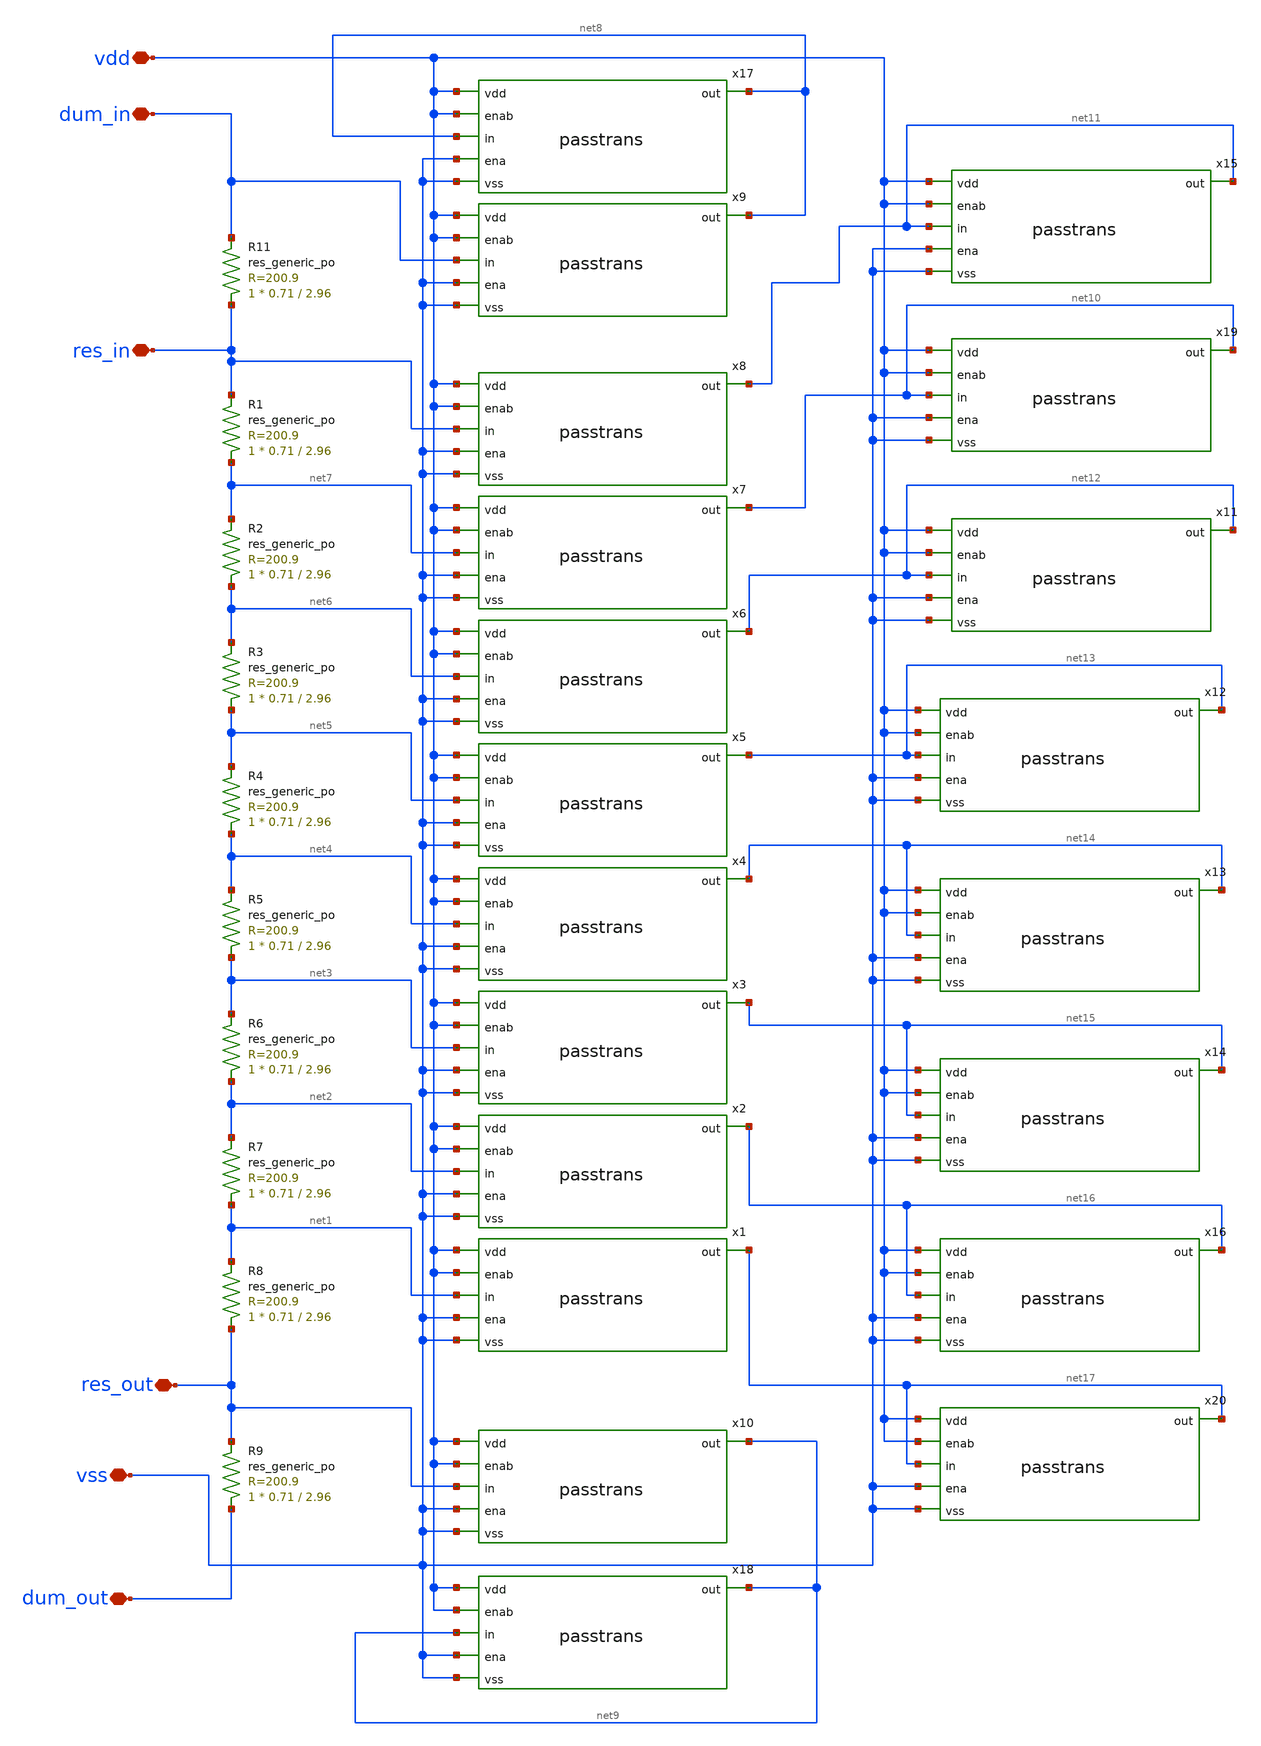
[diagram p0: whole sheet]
** sch_path: xschem/rheo_column_dummy.sch
**.subckt rheo_column_dummy res_in vss vdd dum_in res_out dum_out
*.iopin res_in
*.iopin vss
*.iopin vdd
*.iopin dum_in
*.iopin res_out
*.iopin dum_out
x1 vdd vdd net17 net1 vss vss passtrans
x2 vdd vdd net16 net2 vss vss passtrans
x3 vdd vdd net15 net3 vss vss passtrans
x4 vdd vdd net14 net4 vss vss passtrans
x5 vdd vdd net13 net5 vss vss passtrans
x6 vdd vdd net12 net6 vss vss passtrans
x7 vdd vdd net10 net7 vss vss passtrans
x8 vdd vdd net11 res_in vss vss passtrans
x9 vdd vdd net8 dum_in vss vss passtrans
x10 vdd vdd net9 res_out vss vss passtrans
x11 vdd vdd net12 net12 vss vss passtrans
x12 vdd vdd net13 net13 vss vss passtrans
x13 vdd vdd net14 net14 vss vss passtrans
x14 vdd vdd net15 net15 vss vss passtrans
x15 vdd vdd net11 net11 vss vss passtrans
x16 vdd vdd net16 net16 vss vss passtrans
x17 vdd vdd net8 net8 vss vss passtrans
x18 vdd vdd net9 net9 vss vss passtrans
x19 vdd vdd net10 net10 vss vss passtrans
x20 vdd vdd net17 net17 vss vss passtrans
XR11 res_in dum_in sky130_fd_pr__res_generic_po W=0.71 L=2.96 m=1
XR1 net7 res_in sky130_fd_pr__res_generic_po W=0.71 L=2.96 m=1
XR2 net6 net7 sky130_fd_pr__res_generic_po W=0.71 L=2.96 m=1
XR3 net5 net6 sky130_fd_pr__res_generic_po W=0.71 L=2.96 m=1
XR4 net4 net5 sky130_fd_pr__res_generic_po W=0.71 L=2.96 m=1
XR5 net3 net4 sky130_fd_pr__res_generic_po W=0.71 L=2.96 m=1
XR6 net2 net3 sky130_fd_pr__res_generic_po W=0.71 L=2.96 m=1
XR7 net1 net2 sky130_fd_pr__res_generic_po W=0.71 L=2.96 m=1
XR8 res_out net1 sky130_fd_pr__res_generic_po W=0.71 L=2.96 m=1
XR9 dum_out res_out sky130_fd_pr__res_generic_po W=0.71 L=2.96 m=1
**.ends

* expanding   symbol:  passtrans.sym # of pins=6
** sym_path: xschem/passtrans.sym
** sch_path: xschem/passtrans.sch
.subckt passtrans vdd enab out in ena vss
*.ipin enab
*.ipin ena
*.ipin vss
*.ipin vdd
*.iopin in
*.iopin out
XM1 in ena out vss sky130_fd_pr__nfet_g5v0d10v5 L=0.5 W=0.65 nf=1 ad='int((nf+1)/2) * W/nf * 0.29' as='int((nf+2)/2) * W/nf * 0.29'
+ pd='2*int((nf+1)/2) * (W/nf + 0.29)' ps='2*int((nf+2)/2) * (W/nf + 0.29)' nrd='0.29 / W' nrs='0.29 / W'
+ sa=0 sb=0 sd=0 mult=1 m=1
XM2 in enab out vdd sky130_fd_pr__pfet_g5v0d10v5 L=0.5 W=1 nf=1 ad='int((nf+1)/2) * W/nf * 0.29' as='int((nf+2)/2) * W/nf * 0.29'
+ pd='2*int((nf+1)/2) * (W/nf + 0.29)' ps='2*int((nf+2)/2) * (W/nf + 0.29)' nrd='0.29 / W' nrs='0.29 / W'
+ sa=0 sb=0 sd=0 mult=1 m=1
.ends

.end
